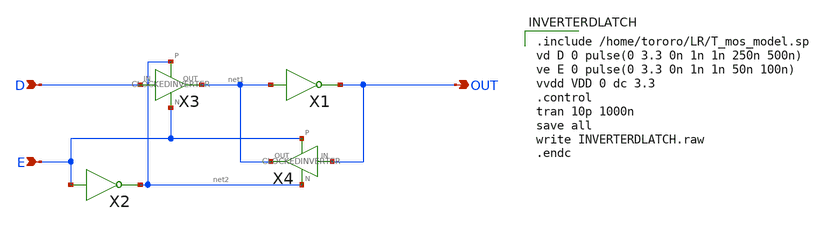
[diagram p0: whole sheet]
** sch_path: task_LATCH/INVERTERDLATCH.sch
**.subckt INVERTERDLATCH D OUT E
*.ipin D
*.opin OUT
*.ipin E
X1 net1 OUT INVERTER
X2 E net2 INVERTER
X3 D net1 net2 E CLOCKEDINVERTER
X4 OUT net1 E net2 CLOCKEDINVERTER
**** begin user architecture code

.include /home/tororo/LR/T_mos_model.sp
vd D 0 pulse(0 3.3 0n 1n 1n 250n 500n)
ve E 0 pulse(0 3.3 0n 1n 1n 50n 100n)
vvdd VDD 0 dc 3.3
.control
tran 10p 1000n
save all
write INVERTERDLATCH.raw
.endc

**** end user architecture code
**.ends

* expanding   symbol:  LR/task_LATCH/INVERTER.sym # of pins=2
** sym_path: task_LATCH/INVERTER.sym
** sch_path: task_LATCH/INVERTER.sch
.subckt INVERTER IN OUT
*.opin OUT
*.ipin IN
M6 OUT IN VDD VDD pch w=10.5u l=0.35u as=0 ps=0 ad=0 pd=0 m=1
M8 OUT IN GND GND nch w=3.5u l=0.35u as=0 ps=0 ad=0 pd=0 m=1
.ends


* expanding   symbol:  LR/task_LATCH/CLOCKEDINVERTER.sym # of pins=4
** sym_path: task_LATCH/CLOCKEDINVERTER.sym
** sch_path: task_LATCH/CLOCKEDINVERTER.sch
.subckt CLOCKEDINVERTER IN OUT P N
*.opin OUT
*.ipin IN
*.ipin P
*.ipin N
M6 OUT IN net1 VDD pch w=10.5u l=0.35u as=0 ps=0 ad=0 pd=0 m=1
M8 OUT IN net2 GND nch w=3.5u l=0.35u as=0 ps=0 ad=0 pd=0 m=1
M1 net1 P VDD VDD pch w=10.5u l=0.35u as=0 ps=0 ad=0 pd=0 m=1
M2 net2 N GND GND nch w=3.5u l=0.35u as=0 ps=0 ad=0 pd=0 m=1
.ends

.GLOBAL VDD
.GLOBAL GND
.end
